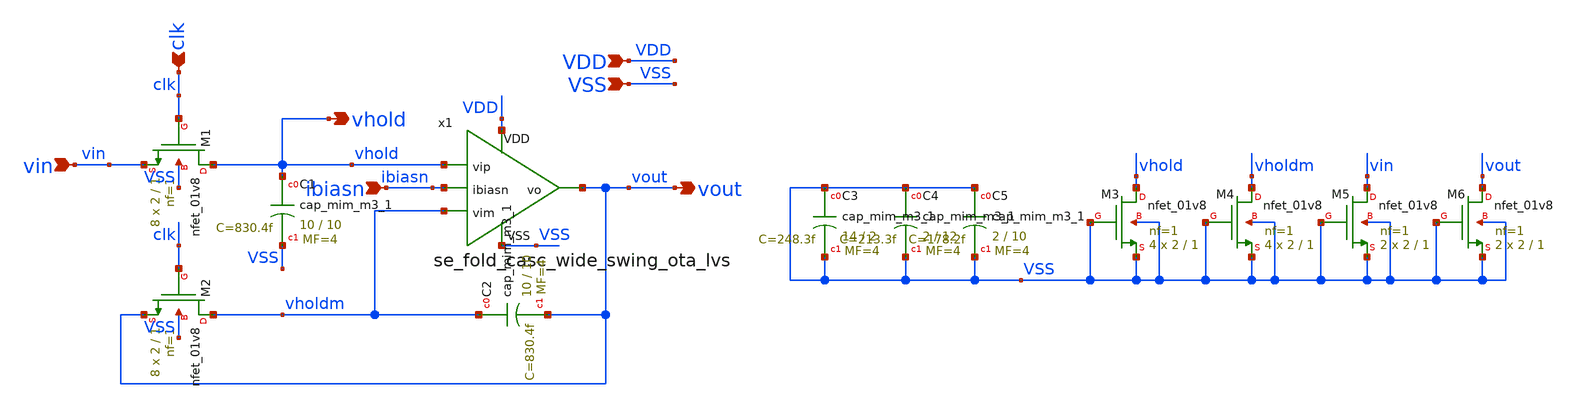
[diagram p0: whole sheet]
** sch_path: designs/sample_and_hold_lvs.sch
* Copyright 2020 Stefan Frederik Schippers
* Licensed under the Apache License, Version 2.0 (the "License");
* you may not use this file except in compliance with the License.
* You may obtain a copy of the License at
* https://www.apache.org/licenses/LICENSE-2.0
* Unless required by applicable law or agreed to in writing, software
* distributed under the License is distributed on an "AS IS" BASIS,
* WITHOUT WARRANTIES OR CONDITIONS OF ANY KIND, either express or implied.
* See the License for the specific language governing permissions and
* limitations under the License.
**.subckt sample_and_hold_lvs vin clk VDD VSS ibiasn vout vhold
*.ipin vin
*.ipin clk
*.ipin VDD
*.ipin VSS
*.ipin ibiasn
*.opin vout
*.opin vhold
XM1 vhold clk vin VSS sky130_fd_pr__nfet_01v8 L=1 W=2 nf=1 ad='int((nf+1)/2) * W/nf * 0.29' as='int((nf+2)/2) * W/nf * 0.29'
+ pd='2*int((nf+1)/2) * (W/nf + 0.29)' ps='2*int((nf+2)/2) * (W/nf + 0.29)' nrd='0.29 / W' nrs='0.29 / W'
+ sa=0 sb=0 sd=0 mult=8 m=8
XM2 vholdm clk vout VSS sky130_fd_pr__nfet_01v8 L=1 W=2 nf=1 ad='int((nf+1)/2) * W/nf * 0.29' as='int((nf+2)/2) * W/nf * 0.29'
+ pd='2*int((nf+1)/2) * (W/nf + 0.29)' ps='2*int((nf+2)/2) * (W/nf + 0.29)' nrd='0.29 / W' nrs='0.29 / W'
+ sa=0 sb=0 sd=0 mult=8 m=8
x1 VSS vout vhold vholdm ibiasn VDD se_fold_casc_wide_swing_ota_lvs
XC1 vhold VSS sky130_fd_pr__cap_mim_m3_1 W=10 L=10 MF=4 m=4
XC2 vholdm vout sky130_fd_pr__cap_mim_m3_1 W=10 L=10 MF=4 m=4
XC3 VSS VSS sky130_fd_pr__cap_mim_m3_1 W=14 L=2 MF=4 m=4
XC4 VSS VSS sky130_fd_pr__cap_mim_m3_1 W=2 L=12 MF=4 m=4
XC5 VSS VSS sky130_fd_pr__cap_mim_m3_1 W=2 L=10 MF=4 m=4
XM3 vhold VSS VSS VSS sky130_fd_pr__nfet_01v8 L=1 W=2 nf=1 ad='int((nf+1)/2) * W/nf * 0.29' as='int((nf+2)/2) * W/nf * 0.29'
+ pd='2*int((nf+1)/2) * (W/nf + 0.29)' ps='2*int((nf+2)/2) * (W/nf + 0.29)' nrd='0.29 / W' nrs='0.29 / W'
+ sa=0 sb=0 sd=0 mult=4 m=4
XM4 vholdm VSS VSS VSS sky130_fd_pr__nfet_01v8 L=1 W=2 nf=1 ad='int((nf+1)/2) * W/nf * 0.29' as='int((nf+2)/2) * W/nf * 0.29'
+ pd='2*int((nf+1)/2) * (W/nf + 0.29)' ps='2*int((nf+2)/2) * (W/nf + 0.29)' nrd='0.29 / W' nrs='0.29 / W'
+ sa=0 sb=0 sd=0 mult=4 m=4
XM5 vin VSS VSS VSS sky130_fd_pr__nfet_01v8 L=1 W=2 nf=1 ad='int((nf+1)/2) * W/nf * 0.29' as='int((nf+2)/2) * W/nf * 0.29'
+ pd='2*int((nf+1)/2) * (W/nf + 0.29)' ps='2*int((nf+2)/2) * (W/nf + 0.29)' nrd='0.29 / W' nrs='0.29 / W'
+ sa=0 sb=0 sd=0 mult=2 m=2
XM6 vout VSS VSS VSS sky130_fd_pr__nfet_01v8 L=1 W=2 nf=1 ad='int((nf+1)/2) * W/nf * 0.29' as='int((nf+2)/2) * W/nf * 0.29'
+ pd='2*int((nf+1)/2) * (W/nf + 0.29)' ps='2*int((nf+2)/2) * (W/nf + 0.29)' nrd='0.29 / W' nrs='0.29 / W'
+ sa=0 sb=0 sd=0 mult=2 m=2
**.ends

* expanding   symbol:
*+  /home/users/nhpoole/ee272b/ee272b_mixed_signal_mmwave_accelerator/designs/se_fold_casc_wide_swing_ota_lvs.sym # of pins=6
** sym_path: designs/se_fold_casc_wide_swing_ota_lvs.sym
** sch_path: designs/se_fold_casc_wide_swing_ota_lvs.sch
.subckt se_fold_casc_wide_swing_ota_lvs VSS vo vip vim ibiasn VDD
*.ipin vip
*.ipin vim
*.opin vo
*.ipin ibiasn
*.ipin VDD
*.ipin VSS
XM11 vmirror vbias3 vcascnm VSS sky130_fd_pr__nfet_01v8 L=4.8 W=3 nf=1 ad='int((nf+1)/2) * W/nf * 0.29'
+ as='int((nf+2)/2) * W/nf * 0.29' pd='2*int((nf+1)/2) * (W/nf + 0.29)' ps='2*int((nf+2)/2) * (W/nf + 0.29)'
+ nrd='0.29 / W' nrs='0.29 / W' sa=0 sb=0 sd=0 mult=18 m=18
XM12 vmirror vbias2 vcascpm VDD sky130_fd_pr__pfet_01v8 L=4.8 W=3 nf=1 ad='int((nf+1)/2) * W/nf * 0.29'
+ as='int((nf+2)/2) * W/nf * 0.29' pd='2*int((nf+1)/2) * (W/nf + 0.29)' ps='2*int((nf+2)/2) * (W/nf + 0.29)'
+ nrd='0.29 / W' nrs='0.29 / W' sa=0 sb=0 sd=0 mult=7 m=7
XM5 vtail_cascn vbias4 VSS VSS sky130_fd_pr__nfet_01v8 L=4.8 W=3 nf=1 ad='int((nf+1)/2) * W/nf * 0.29'
+ as='int((nf+2)/2) * W/nf * 0.29' pd='2*int((nf+1)/2) * (W/nf + 0.29)' ps='2*int((nf+2)/2) * (W/nf + 0.29)'
+ nrd='0.29 / W' nrs='0.29 / W' sa=0 sb=0 sd=0 mult=36 m=36
XM6 vtail_cascp vbias1 VDD VDD sky130_fd_pr__pfet_01v8_lvt L=4.8 W=3 nf=1 ad='int((nf+1)/2) * W/nf * 0.29'
+ as='int((nf+2)/2) * W/nf * 0.29' pd='2*int((nf+1)/2) * (W/nf + 0.29)' ps='2*int((nf+2)/2) * (W/nf + 0.29)'
+ nrd='0.29 / W' nrs='0.29 / W' sa=0 sb=0 sd=0 mult=12 m=12
XM3 vcascnm vip vtail_cascp VDD sky130_fd_pr__pfet_01v8_lvt L=4.8 W=3 nf=1 ad='int((nf+1)/2) * W/nf * 0.29'
+ as='int((nf+2)/2) * W/nf * 0.29' pd='2*int((nf+1)/2) * (W/nf + 0.29)' ps='2*int((nf+2)/2) * (W/nf + 0.29)'
+ nrd='0.29 / W' nrs='0.29 / W' sa=0 sb=0 sd=0 mult=4 m=4
XM1 vcascpm vip vtail_cascn VSS sky130_fd_pr__nfet_01v8_lvt L=4.8 W=3 nf=1 ad='int((nf+1)/2) * W/nf * 0.29'
+ as='int((nf+2)/2) * W/nf * 0.29' pd='2*int((nf+1)/2) * (W/nf + 0.29)' ps='2*int((nf+2)/2) * (W/nf + 0.29)'
+ nrd='0.29 / W' nrs='0.29 / W' sa=0 sb=0 sd=0 mult=18 m=18
XM7 M7d vbias1 VDD VDD sky130_fd_pr__pfet_01v8_lvt L=4.8 W=3 nf=1 ad='int((nf+1)/2) * W/nf * 0.29' as='int((nf+2)/2) * W/nf * 0.29'
+ pd='2*int((nf+1)/2) * (W/nf + 0.29)' ps='2*int((nf+2)/2) * (W/nf + 0.29)' nrd='0.29 / W' nrs='0.29 / W'
+ sa=0 sb=0 sd=0 mult=6 m=6
XM8 M8d vbias2 M9d VDD sky130_fd_pr__pfet_01v8 L=4.8 W=3 nf=1 ad='int((nf+1)/2) * W/nf * 0.29' as='int((nf+2)/2) * W/nf * 0.29'
+ pd='2*int((nf+1)/2) * (W/nf + 0.29)' ps='2*int((nf+2)/2) * (W/nf + 0.29)' nrd='0.29 / W' nrs='0.29 / W'
+ sa=0 sb=0 sd=0 mult=6 m=6
XM9 M9d vbias1 VDD VDD sky130_fd_pr__pfet_01v8_lvt L=4.8 W=3 nf=1 ad='int((nf+1)/2) * W/nf * 0.29' as='int((nf+2)/2) * W/nf * 0.29'
+ pd='2*int((nf+1)/2) * (W/nf + 0.29)' ps='2*int((nf+2)/2) * (W/nf + 0.29)' nrd='0.29 / W' nrs='0.29 / W'
+ sa=0 sb=0 sd=0 mult=6 m=6
XM13 M13d vbias1 VDD VDD sky130_fd_pr__pfet_01v8_lvt L=4.8 W=3 nf=1 ad='int((nf+1)/2) * W/nf * 0.29'
+ as='int((nf+2)/2) * W/nf * 0.29' pd='2*int((nf+1)/2) * (W/nf + 0.29)' ps='2*int((nf+2)/2) * (W/nf + 0.29)'
+ nrd='0.29 / W' nrs='0.29 / W' sa=0 sb=0 sd=0 mult=6 m=6
XM14 vbias1 vbias2 M7d VDD sky130_fd_pr__pfet_01v8 L=4.8 W=3 nf=1 ad='int((nf+1)/2) * W/nf * 0.29' as='int((nf+2)/2) * W/nf * 0.29'
+ pd='2*int((nf+1)/2) * (W/nf + 0.29)' ps='2*int((nf+2)/2) * (W/nf + 0.29)' nrd='0.29 / W' nrs='0.29 / W'
+ sa=0 sb=0 sd=0 mult=6 m=6
XM16 M16d vbias2 M13d VDD sky130_fd_pr__pfet_01v8 L=4.8 W=3 nf=1 ad='int((nf+1)/2) * W/nf * 0.29' as='int((nf+2)/2) * W/nf * 0.29'
+ pd='2*int((nf+1)/2) * (W/nf + 0.29)' ps='2*int((nf+2)/2) * (W/nf + 0.29)' nrd='0.29 / W' nrs='0.29 / W'
+ sa=0 sb=0 sd=0 mult=6 m=6
XM26 vbias2 ibiasn VSS VSS sky130_fd_pr__nfet_01v8 L=4.8 W=3 nf=1 ad='int((nf+1)/2) * W/nf * 0.29' as='int((nf+2)/2) * W/nf * 0.29'
+ pd='2*int((nf+1)/2) * (W/nf + 0.29)' ps='2*int((nf+2)/2) * (W/nf + 0.29)' nrd='0.29 / W' nrs='0.29 / W'
+ sa=0 sb=0 sd=0 mult=4 m=4
XM17 vbias1 vbias1 vbias2 VSS sky130_fd_pr__nfet_01v8_lvt L=4.8 W=3 nf=1 ad='int((nf+1)/2) * W/nf * 0.29'
+ as='int((nf+2)/2) * W/nf * 0.29' pd='2*int((nf+1)/2) * (W/nf + 0.29)' ps='2*int((nf+2)/2) * (W/nf + 0.29)'
+ nrd='0.29 / W' nrs='0.29 / W' sa=0 sb=0 sd=0 mult=56 m=56
XM10 vcascnp vbias4 VSS VSS sky130_fd_pr__nfet_01v8 L=4.8 W=3 nf=1 ad='int((nf+1)/2) * W/nf * 0.29' as='int((nf+2)/2) * W/nf * 0.29'
+ pd='2*int((nf+1)/2) * (W/nf + 0.29)' ps='2*int((nf+2)/2) * (W/nf + 0.29)' nrd='0.29 / W' nrs='0.29 / W'
+ sa=0 sb=0 sd=0 mult=36 m=36
XM18 vcascnm vbias4 VSS VSS sky130_fd_pr__nfet_01v8 L=4.8 W=3 nf=1 ad='int((nf+1)/2) * W/nf * 0.29' as='int((nf+2)/2) * W/nf * 0.29'
+ pd='2*int((nf+1)/2) * (W/nf + 0.29)' ps='2*int((nf+2)/2) * (W/nf + 0.29)' nrd='0.29 / W' nrs='0.29 / W'
+ sa=0 sb=0 sd=0 mult=36 m=36
XM4 vcascpp vim vtail_cascn VSS sky130_fd_pr__nfet_01v8_lvt L=4.8 W=3 nf=1 ad='int((nf+1)/2) * W/nf * 0.29'
+ as='int((nf+2)/2) * W/nf * 0.29' pd='2*int((nf+1)/2) * (W/nf + 0.29)' ps='2*int((nf+2)/2) * (W/nf + 0.29)'
+ nrd='0.29 / W' nrs='0.29 / W' sa=0 sb=0 sd=0 mult=18 m=18
XM2 vcascnp vim vtail_cascp VDD sky130_fd_pr__pfet_01v8_lvt L=4.8 W=3 nf=1 ad='int((nf+1)/2) * W/nf * 0.29'
+ as='int((nf+2)/2) * W/nf * 0.29' pd='2*int((nf+1)/2) * (W/nf + 0.29)' ps='2*int((nf+2)/2) * (W/nf + 0.29)'
+ nrd='0.29 / W' nrs='0.29 / W' sa=0 sb=0 sd=0 mult=4 m=4
XM15 vcascpp vmirror VDD VDD sky130_fd_pr__pfet_01v8_lvt L=4.8 W=3 nf=1 ad='int((nf+1)/2) * W/nf * 0.29'
+ as='int((nf+2)/2) * W/nf * 0.29' pd='2*int((nf+1)/2) * (W/nf + 0.29)' ps='2*int((nf+2)/2) * (W/nf + 0.29)'
+ nrd='0.29 / W' nrs='0.29 / W' sa=0 sb=0 sd=0 mult=12 m=12
XM19 vcascpm vmirror VDD VDD sky130_fd_pr__pfet_01v8_lvt L=4.8 W=3 nf=1 ad='int((nf+1)/2) * W/nf * 0.29'
+ as='int((nf+2)/2) * W/nf * 0.29' pd='2*int((nf+1)/2) * (W/nf + 0.29)' ps='2*int((nf+2)/2) * (W/nf + 0.29)'
+ nrd='0.29 / W' nrs='0.29 / W' sa=0 sb=0 sd=0 mult=12 m=12
XM20 M21d vbias4 VSS VSS sky130_fd_pr__nfet_01v8 L=4.8 W=3 nf=1 ad='int((nf+1)/2) * W/nf * 0.29' as='int((nf+2)/2) * W/nf * 0.29'
+ pd='2*int((nf+1)/2) * (W/nf + 0.29)' ps='2*int((nf+2)/2) * (W/nf + 0.29)' nrd='0.29 / W' nrs='0.29 / W'
+ sa=0 sb=0 sd=0 mult=18 m=18
XM21 vbias4 vbias3 M21d VSS sky130_fd_pr__nfet_01v8 L=4.8 W=3 nf=1 ad='int((nf+1)/2) * W/nf * 0.29' as='int((nf+2)/2) * W/nf * 0.29'
+ pd='2*int((nf+1)/2) * (W/nf + 0.29)' ps='2*int((nf+2)/2) * (W/nf + 0.29)' nrd='0.29 / W' nrs='0.29 / W'
+ sa=0 sb=0 sd=0 mult=18 m=18
XM22 M8d M8d vbias3 VSS sky130_fd_pr__nfet_01v8 L=4.8 W=3 nf=1 ad='int((nf+1)/2) * W/nf * 0.29' as='int((nf+2)/2) * W/nf * 0.29'
+ pd='2*int((nf+1)/2) * (W/nf + 0.29)' ps='2*int((nf+2)/2) * (W/nf + 0.29)' nrd='0.29 / W' nrs='0.29 / W'
+ sa=0 sb=0 sd=0 mult=40 m=40
XM23 vbias3 M8d vbias4 VSS sky130_fd_pr__nfet_01v8 L=4.8 W=3 nf=1 ad='int((nf+1)/2) * W/nf * 0.29' as='int((nf+2)/2) * W/nf * 0.29'
+ pd='2*int((nf+1)/2) * (W/nf + 0.29)' ps='2*int((nf+2)/2) * (W/nf + 0.29)' nrd='0.29 / W' nrs='0.29 / W'
+ sa=0 sb=0 sd=0 mult=2 m=2
XM24 vo vbias3 vcascnp VSS sky130_fd_pr__nfet_01v8 L=4.8 W=3 nf=1 ad='int((nf+1)/2) * W/nf * 0.29' as='int((nf+2)/2) * W/nf * 0.29'
+ pd='2*int((nf+1)/2) * (W/nf + 0.29)' ps='2*int((nf+2)/2) * (W/nf + 0.29)' nrd='0.29 / W' nrs='0.29 / W'
+ sa=0 sb=0 sd=0 mult=18 m=18
XM25 ibiasn ibiasn VSS VSS sky130_fd_pr__nfet_01v8 L=4.8 W=3 nf=1 ad='int((nf+1)/2) * W/nf * 0.29' as='int((nf+2)/2) * W/nf * 0.29'
+ pd='2*int((nf+1)/2) * (W/nf + 0.29)' ps='2*int((nf+2)/2) * (W/nf + 0.29)' nrd='0.29 / W' nrs='0.29 / W'
+ sa=0 sb=0 sd=0 mult=4 m=4
XM27 M16d M16d VSS VSS sky130_fd_pr__nfet_01v8 L=4.8 W=3 nf=1 ad='int((nf+1)/2) * W/nf * 0.29' as='int((nf+2)/2) * W/nf * 0.29'
+ pd='2*int((nf+1)/2) * (W/nf + 0.29)' ps='2*int((nf+2)/2) * (W/nf + 0.29)' nrd='0.29 / W' nrs='0.29 / W'
+ sa=0 sb=0 sd=0 mult=1 m=1
XM28 vo vbias2 vcascpp VDD sky130_fd_pr__pfet_01v8 L=4.8 W=3 nf=1 ad='int((nf+1)/2) * W/nf * 0.29' as='int((nf+2)/2) * W/nf * 0.29'
+ pd='2*int((nf+1)/2) * (W/nf + 0.29)' ps='2*int((nf+2)/2) * (W/nf + 0.29)' nrd='0.29 / W' nrs='0.29 / W'
+ sa=0 sb=0 sd=0 mult=7 m=7
XM29 vbias1 VDD VDD VDD sky130_fd_pr__pfet_01v8 L=4.8 W=3 nf=1 ad='int((nf+1)/2) * W/nf * 0.29' as='int((nf+2)/2) * W/nf * 0.29'
+ pd='2*int((nf+1)/2) * (W/nf + 0.29)' ps='2*int((nf+2)/2) * (W/nf + 0.29)' nrd='0.29 / W' nrs='0.29 / W'
+ sa=0 sb=0 sd=0 mult=2 m=2
XM31 M8d VDD VDD VDD sky130_fd_pr__pfet_01v8 L=4.8 W=3 nf=1 ad='int((nf+1)/2) * W/nf * 0.29' as='int((nf+2)/2) * W/nf * 0.29'
+ pd='2*int((nf+1)/2) * (W/nf + 0.29)' ps='2*int((nf+2)/2) * (W/nf + 0.29)' nrd='0.29 / W' nrs='0.29 / W'
+ sa=0 sb=0 sd=0 mult=2 m=2
XM32 vcascpp VDD VDD VDD sky130_fd_pr__pfet_01v8 L=4.8 W=3 nf=1 ad='int((nf+1)/2) * W/nf * 0.29' as='int((nf+2)/2) * W/nf * 0.29'
+ pd='2*int((nf+1)/2) * (W/nf + 0.29)' ps='2*int((nf+2)/2) * (W/nf + 0.29)' nrd='0.29 / W' nrs='0.29 / W'
+ sa=0 sb=0 sd=0 mult=3 m=3
XM33 vcascpm VDD VDD VDD sky130_fd_pr__pfet_01v8 L=4.8 W=3 nf=1 ad='int((nf+1)/2) * W/nf * 0.29' as='int((nf+2)/2) * W/nf * 0.29'
+ pd='2*int((nf+1)/2) * (W/nf + 0.29)' ps='2*int((nf+2)/2) * (W/nf + 0.29)' nrd='0.29 / W' nrs='0.29 / W'
+ sa=0 sb=0 sd=0 mult=3 m=3
XM34 M16d VDD VDD VDD sky130_fd_pr__pfet_01v8 L=4.8 W=3 nf=1 ad='int((nf+1)/2) * W/nf * 0.29' as='int((nf+2)/2) * W/nf * 0.29'
+ pd='2*int((nf+1)/2) * (W/nf + 0.29)' ps='2*int((nf+2)/2) * (W/nf + 0.29)' nrd='0.29 / W' nrs='0.29 / W'
+ sa=0 sb=0 sd=0 mult=2 m=2
XM35 M13d VDD VDD VDD sky130_fd_pr__pfet_01v8 L=4.8 W=3 nf=1 ad='int((nf+1)/2) * W/nf * 0.29' as='int((nf+2)/2) * W/nf * 0.29'
+ pd='2*int((nf+1)/2) * (W/nf + 0.29)' ps='2*int((nf+2)/2) * (W/nf + 0.29)' nrd='0.29 / W' nrs='0.29 / W'
+ sa=0 sb=0 sd=0 mult=2 m=2
XM39 M7d M7d M7d VDD sky130_fd_pr__pfet_01v8 L=4.8 W=3 nf=1 ad='int((nf+1)/2) * W/nf * 0.29' as='int((nf+2)/2) * W/nf * 0.29'
+ pd='2*int((nf+1)/2) * (W/nf + 0.29)' ps='2*int((nf+2)/2) * (W/nf + 0.29)' nrd='0.29 / W' nrs='0.29 / W'
+ sa=0 sb=0 sd=0 mult=2 m=2
XM40 VSS VSS VSS VSS sky130_fd_pr__nfet_01v8 L=4.8 W=3 nf=1 ad='int((nf+1)/2) * W/nf * 0.29' as='int((nf+2)/2) * W/nf * 0.29'
+ pd='2*int((nf+1)/2) * (W/nf + 0.29)' ps='2*int((nf+2)/2) * (W/nf + 0.29)' nrd='0.29 / W' nrs='0.29 / W'
+ sa=0 sb=0 sd=0 mult=5 m=5
XM41 vo vo vo VSS sky130_fd_pr__nfet_01v8 L=4.8 W=3 nf=1 ad='int((nf+1)/2) * W/nf * 0.29' as='int((nf+2)/2) * W/nf * 0.29'
+ pd='2*int((nf+1)/2) * (W/nf + 0.29)' ps='2*int((nf+2)/2) * (W/nf + 0.29)' nrd='0.29 / W' nrs='0.29 / W'
+ sa=0 sb=0 sd=0 mult=2 m=2
XM42 M9d M9d M9d VDD sky130_fd_pr__pfet_01v8 L=4.8 W=3 nf=1 ad='int((nf+1)/2) * W/nf * 0.29' as='int((nf+2)/2) * W/nf * 0.29'
+ pd='2*int((nf+1)/2) * (W/nf + 0.29)' ps='2*int((nf+2)/2) * (W/nf + 0.29)' nrd='0.29 / W' nrs='0.29 / W'
+ sa=0 sb=0 sd=0 mult=2 m=2
XM51 vo vo vo VDD sky130_fd_pr__pfet_01v8 L=4.8 W=3 nf=1 ad='int((nf+1)/2) * W/nf * 0.29' as='int((nf+2)/2) * W/nf * 0.29'
+ pd='2*int((nf+1)/2) * (W/nf + 0.29)' ps='2*int((nf+2)/2) * (W/nf + 0.29)' nrd='0.29 / W' nrs='0.29 / W'
+ sa=0 sb=0 sd=0 mult=2 m=2
XM52 vmirror vmirror vmirror VDD sky130_fd_pr__pfet_01v8 L=4.8 W=3 nf=1 ad='int((nf+1)/2) * W/nf * 0.29'
+ as='int((nf+2)/2) * W/nf * 0.29' pd='2*int((nf+1)/2) * (W/nf + 0.29)' ps='2*int((nf+2)/2) * (W/nf + 0.29)'
+ nrd='0.29 / W' nrs='0.29 / W' sa=0 sb=0 sd=0 mult=2 m=2
XM53 vmirror vmirror vmirror VSS sky130_fd_pr__nfet_01v8 L=4.8 W=3 nf=1 ad='int((nf+1)/2) * W/nf * 0.29'
+ as='int((nf+2)/2) * W/nf * 0.29' pd='2*int((nf+1)/2) * (W/nf + 0.29)' ps='2*int((nf+2)/2) * (W/nf + 0.29)'
+ nrd='0.29 / W' nrs='0.29 / W' sa=0 sb=0 sd=0 mult=2 m=2
XM54 M9d M9d M9d VDD sky130_fd_pr__pfet_01v8_lvt L=4.8 W=3 nf=1 ad='int((nf+1)/2) * W/nf * 0.29' as='int((nf+2)/2) * W/nf * 0.29'
+ pd='2*int((nf+1)/2) * (W/nf + 0.29)' ps='2*int((nf+2)/2) * (W/nf + 0.29)' nrd='0.29 / W' nrs='0.29 / W'
+ sa=0 sb=0 sd=0 mult=2 m=2
XM55 M7d M7d M7d VDD sky130_fd_pr__pfet_01v8_lvt L=4.8 W=3 nf=1 ad='int((nf+1)/2) * W/nf * 0.29' as='int((nf+2)/2) * W/nf * 0.29'
+ pd='2*int((nf+1)/2) * (W/nf + 0.29)' ps='2*int((nf+2)/2) * (W/nf + 0.29)' nrd='0.29 / W' nrs='0.29 / W'
+ sa=0 sb=0 sd=0 mult=2 m=2
XM43 M13d M13d M13d VDD sky130_fd_pr__pfet_01v8_lvt L=4.8 W=3 nf=1 ad='int((nf+1)/2) * W/nf * 0.29' as='int((nf+2)/2) * W/nf * 0.29'
+ pd='2*int((nf+1)/2) * (W/nf + 0.29)' ps='2*int((nf+2)/2) * (W/nf + 0.29)' nrd='0.29 / W' nrs='0.29 / W'
+ sa=0 sb=0 sd=0 mult=2 m=2
XM58 vtail_cascn vtail_cascn vtail_cascn VSS sky130_fd_pr__nfet_01v8 L=4.8 W=3 nf=1 ad='int((nf+1)/2) * W/nf * 0.29'
+ as='int((nf+2)/2) * W/nf * 0.29' pd='2*int((nf+1)/2) * (W/nf + 0.29)' ps='2*int((nf+2)/2) * (W/nf + 0.29)'
+ nrd='0.29 / W' nrs='0.29 / W' sa=0 sb=0 sd=0 mult=4 m=4
XM60 vtail_cascn vtail_cascn vtail_cascn VSS sky130_fd_pr__nfet_01v8_lvt L=4.8 W=3 nf=1 ad='int((nf+1)/2) * W/nf * 0.29'
+ as='int((nf+2)/2) * W/nf * 0.29' pd='2*int((nf+1)/2) * (W/nf + 0.29)' ps='2*int((nf+2)/2) * (W/nf + 0.29)'
+ nrd='0.29 / W' nrs='0.29 / W' sa=0 sb=0 sd=0 mult=4 m=4
XM61 vcascpm vcascpm vcascpm VSS sky130_fd_pr__nfet_01v8_lvt L=4.8 W=3 nf=1 ad='int((nf+1)/2) * W/nf * 0.29'
+ as='int((nf+2)/2) * W/nf * 0.29' pd='2*int((nf+1)/2) * (W/nf + 0.29)' ps='2*int((nf+2)/2) * (W/nf + 0.29)'
+ nrd='0.29 / W' nrs='0.29 / W' sa=0 sb=0 sd=0 mult=2 m=2
XM62 vcascpp vcascpp vcascpp VSS sky130_fd_pr__nfet_01v8_lvt L=4.8 W=3 nf=1 ad='int((nf+1)/2) * W/nf * 0.29'
+ as='int((nf+2)/2) * W/nf * 0.29' pd='2*int((nf+1)/2) * (W/nf + 0.29)' ps='2*int((nf+2)/2) * (W/nf + 0.29)'
+ nrd='0.29 / W' nrs='0.29 / W' sa=0 sb=0 sd=0 mult=2 m=2
XM66 ibiasn ibiasn ibiasn VSS sky130_fd_pr__nfet_01v8 L=4.8 W=3 nf=1 ad='int((nf+1)/2) * W/nf * 0.29'
+ as='int((nf+2)/2) * W/nf * 0.29' pd='2*int((nf+1)/2) * (W/nf + 0.29)' ps='2*int((nf+2)/2) * (W/nf + 0.29)'
+ nrd='0.29 / W' nrs='0.29 / W' sa=0 sb=0 sd=0 mult=2 m=2
XM67 vbias2 vbias2 vbias2 VSS sky130_fd_pr__nfet_01v8_lvt L=4.8 W=3 nf=1 ad='int((nf+1)/2) * W/nf * 0.29'
+ as='int((nf+2)/2) * W/nf * 0.29' pd='2*int((nf+1)/2) * (W/nf + 0.29)' ps='2*int((nf+2)/2) * (W/nf + 0.29)'
+ nrd='0.29 / W' nrs='0.29 / W' sa=0 sb=0 sd=0 mult=8 m=8
XM68 vbias1 vbias1 vbias1 VSS sky130_fd_pr__nfet_01v8_lvt L=4.8 W=3 nf=1 ad='int((nf+1)/2) * W/nf * 0.29'
+ as='int((nf+2)/2) * W/nf * 0.29' pd='2*int((nf+1)/2) * (W/nf + 0.29)' ps='2*int((nf+2)/2) * (W/nf + 0.29)'
+ nrd='0.29 / W' nrs='0.29 / W' sa=0 sb=0 sd=0 mult=8 m=8
XC3 VSS VSS sky130_fd_pr__cap_mim_m3_1 W=31 L=2 MF=4 m=4
XC4 VSS VSS sky130_fd_pr__cap_mim_m3_1 W=4 L=29 MF=4 m=4
XC1 vo VSS sky130_fd_pr__cap_mim_m3_1 W=26 L=24 MF=4 m=4
XM44 vcascpm vcascpm vcascpm VDD sky130_fd_pr__pfet_01v8_lvt L=4.8 W=3 nf=1 ad='int((nf+1)/2) * W/nf * 0.29'
+ as='int((nf+2)/2) * W/nf * 0.29' pd='2*int((nf+1)/2) * (W/nf + 0.29)' ps='2*int((nf+2)/2) * (W/nf + 0.29)'
+ nrd='0.29 / W' nrs='0.29 / W' sa=0 sb=0 sd=0 mult=2 m=2
XM45 vcascpp vcascpp vcascpp VDD sky130_fd_pr__pfet_01v8_lvt L=4.8 W=3 nf=1 ad='int((nf+1)/2) * W/nf * 0.29'
+ as='int((nf+2)/2) * W/nf * 0.29' pd='2*int((nf+1)/2) * (W/nf + 0.29)' ps='2*int((nf+2)/2) * (W/nf + 0.29)'
+ nrd='0.29 / W' nrs='0.29 / W' sa=0 sb=0 sd=0 mult=2 m=2
XM46 vo VDD VDD VDD sky130_fd_pr__pfet_01v8 L=4.8 W=3 nf=1 ad='int((nf+1)/2) * W/nf * 0.29' as='int((nf+2)/2) * W/nf * 0.29'
+ pd='2*int((nf+1)/2) * (W/nf + 0.29)' ps='2*int((nf+2)/2) * (W/nf + 0.29)' nrd='0.29 / W' nrs='0.29 / W'
+ sa=0 sb=0 sd=0 mult=1 m=1
XM47 vmirror VDD VDD VDD sky130_fd_pr__pfet_01v8 L=4.8 W=3 nf=1 ad='int((nf+1)/2) * W/nf * 0.29' as='int((nf+2)/2) * W/nf * 0.29'
+ pd='2*int((nf+1)/2) * (W/nf + 0.29)' ps='2*int((nf+2)/2) * (W/nf + 0.29)' nrd='0.29 / W' nrs='0.29 / W'
+ sa=0 sb=0 sd=0 mult=1 m=1
XM48 vcascnm vcascnm vcascnm VDD sky130_fd_pr__pfet_01v8_lvt L=4.8 W=3 nf=1 ad='int((nf+1)/2) * W/nf * 0.29'
+ as='int((nf+2)/2) * W/nf * 0.29' pd='2*int((nf+1)/2) * (W/nf + 0.29)' ps='2*int((nf+2)/2) * (W/nf + 0.29)'
+ nrd='0.29 / W' nrs='0.29 / W' sa=0 sb=0 sd=0 mult=4 m=4
XM49 vcascnp vcascnp vcascnp VDD sky130_fd_pr__pfet_01v8_lvt L=4.8 W=3 nf=1 ad='int((nf+1)/2) * W/nf * 0.29'
+ as='int((nf+2)/2) * W/nf * 0.29' pd='2*int((nf+1)/2) * (W/nf + 0.29)' ps='2*int((nf+2)/2) * (W/nf + 0.29)'
+ nrd='0.29 / W' nrs='0.29 / W' sa=0 sb=0 sd=0 mult=4 m=4
XM36 vcascnp vcascnp vcascnp VSS sky130_fd_pr__nfet_01v8 L=4.8 W=3 nf=1 ad='int((nf+1)/2) * W/nf * 0.29'
+ as='int((nf+2)/2) * W/nf * 0.29' pd='2*int((nf+1)/2) * (W/nf + 0.29)' ps='2*int((nf+2)/2) * (W/nf + 0.29)'
+ nrd='0.29 / W' nrs='0.29 / W' sa=0 sb=0 sd=0 mult=2 m=2
XM50 vcascnm vcascnm vcascnm VSS sky130_fd_pr__nfet_01v8 L=4.8 W=3 nf=1 ad='int((nf+1)/2) * W/nf * 0.29'
+ as='int((nf+2)/2) * W/nf * 0.29' pd='2*int((nf+1)/2) * (W/nf + 0.29)' ps='2*int((nf+2)/2) * (W/nf + 0.29)'
+ nrd='0.29 / W' nrs='0.29 / W' sa=0 sb=0 sd=0 mult=2 m=2
XM37 VDD VDD VDD VDD sky130_fd_pr__pfet_01v8 L=4.8 W=3 nf=1 ad='int((nf+1)/2) * W/nf * 0.29' as='int((nf+2)/2) * W/nf * 0.29'
+ pd='2*int((nf+1)/2) * (W/nf + 0.29)' ps='2*int((nf+2)/2) * (W/nf + 0.29)' nrd='0.29 / W' nrs='0.29 / W'
+ sa=0 sb=0 sd=0 mult=4 m=4
XM30 VDD VDD VDD VDD sky130_fd_pr__pfet_01v8_lvt L=4.8 W=3 nf=1 ad='int((nf+1)/2) * W/nf * 0.29' as='int((nf+2)/2) * W/nf * 0.29'
+ pd='2*int((nf+1)/2) * (W/nf + 0.29)' ps='2*int((nf+2)/2) * (W/nf + 0.29)' nrd='0.29 / W' nrs='0.29 / W'
+ sa=0 sb=0 sd=0 mult=12 m=12
XC2 VSS vo sky130_fd_pr__cap_mim_m3_2 W=24 L=26 MF=4 m=4
XC5 VSS VSS sky130_fd_pr__cap_mim_m3_2 W=29 L=4 MF=4 m=4
XC6 VSS VSS sky130_fd_pr__cap_mim_m3_2 W=2 L=31 MF=4 m=4
.ends

.end
